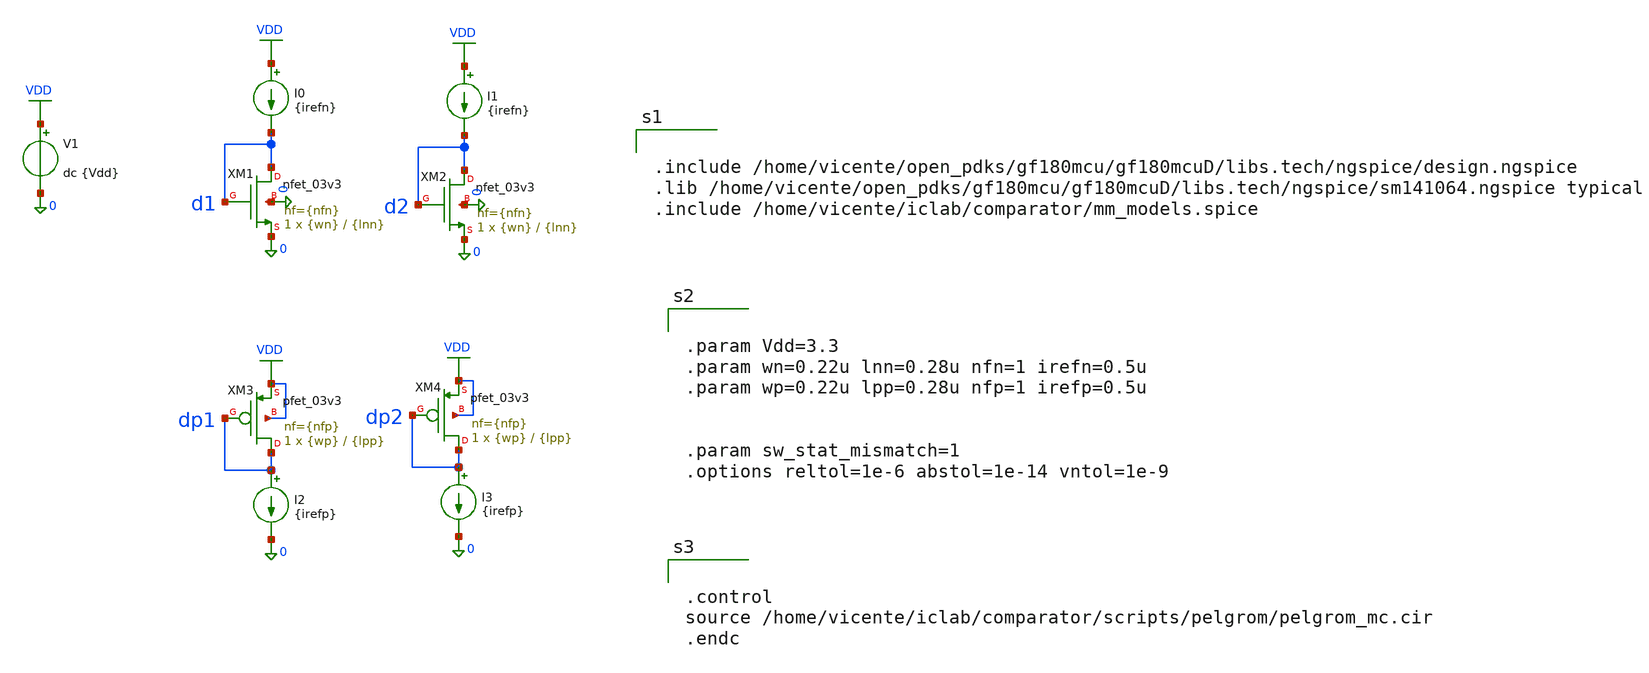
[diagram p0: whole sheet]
** sch_path: comparator/pelgrom.sch
**.subckt pelgrom
XM1 d1 d1 0 0 nfet_03v3 L={lnn} W={wn} nf={nfn} ad='int((nf+1)/2) * W/nf * 0.18u' as='int((nf+2)/2) * W/nf * 0.18u'
+ pd='2*int((nf+1)/2) * (W/nf + 0.18u)' ps='2*int((nf+2)/2) * (W/nf + 0.18u)' nrd='0.18u / W' nrs='0.18u / W'
+ sa=0 sb=0 sd=0 m=1
I0 VDD d1 {irefn}
V1 VDD 0 dc {Vdd}
XM2 d2 d2 0 0 nfet_03v3 L={lnn} W={wn} nf={nfn} ad='int((nf+1)/2) * W/nf * 0.18u' as='int((nf+2)/2) * W/nf * 0.18u'
+ pd='2*int((nf+1)/2) * (W/nf + 0.18u)' ps='2*int((nf+2)/2) * (W/nf + 0.18u)' nrd='0.18u / W' nrs='0.18u / W'
+ sa=0 sb=0 sd=0 m=1
I1 VDD d2 {irefn}
XM3 dp1 dp1 VDD VDD pfet_03v3 L={lpp} W={wp} nf={nfp} ad='int((nf+1)/2) * W/nf * 0.18u' as='int((nf+2)/2) * W/nf * 0.18u'
+ pd='2*int((nf+1)/2) * (W/nf + 0.18u)' ps='2*int((nf+2)/2) * (W/nf + 0.18u)' nrd='0.18u / W' nrs='0.18u / W'
+ sa=0 sb=0 sd=0 m=1
I2 dp1 0 {irefp}
XM4 dp2 dp2 VDD VDD pfet_03v3 L={lpp} W={wp} nf={nfp} ad='int((nf+1)/2) * W/nf * 0.18u' as='int((nf+2)/2) * W/nf * 0.18u'
+ pd='2*int((nf+1)/2) * (W/nf + 0.18u)' ps='2*int((nf+2)/2) * (W/nf + 0.18u)' nrd='0.18u / W' nrs='0.18u / W'
+ sa=0 sb=0 sd=0 m=1
I3 dp2 0 {irefp}
**** begin user architecture code


.include /home/vicente/open_pdks/gf180mcu/gf180mcuD/libs.tech/ngspice/design.ngspice
.lib /home/vicente/open_pdks/gf180mcu/gf180mcuD/libs.tech/ngspice/sm141064.ngspice typical
.include /home/vicente/iclab/comparator/mm_models.spice




.param Vdd=3.3
.param wn=0.22u lnn=0.28u nfn=1 irefn=0.5u
.param wp=0.22u lpp=0.28u nfp=1 irefp=0.5u


.param sw_stat_mismatch=1
.options reltol=1e-6 abstol=1e-14 vntol=1e-9




.control
source /home/vicente/iclab/comparator/scripts/pelgrom/pelgrom_mc.cir
.endc


**** end user architecture code
**.ends
.GLOBAL VDD
.end
